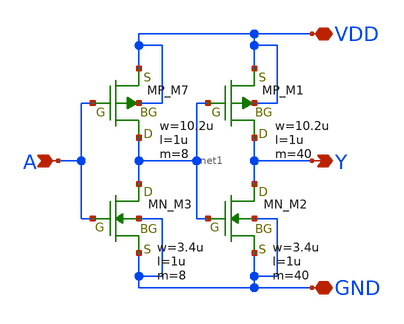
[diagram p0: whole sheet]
** sch_path: libs.tech/xschem/TR-1um_5_stdcell/CLKBUF_X8.sch
**.subckt CLKBUF_X8 A Y VDD GND
*.ipin A
*.opin Y
*.iopin VDD
*.iopin GND
XM7 net1 A VDD VDD PMOS w=10.2u l=1u nrd=0 nrs=0 m=8
XM1 Y net1 VDD VDD PMOS w=10.2u l=1u nrd=0 nrs=0 m=40
XM3 net1 A GND GND NMOS w=3.4u l=1u nrd=0 nrs=0 m=8
XM2 Y net1 GND GND NMOS w=3.4u l=1u nrd=0 nrs=0 m=40
**.ends
.end
